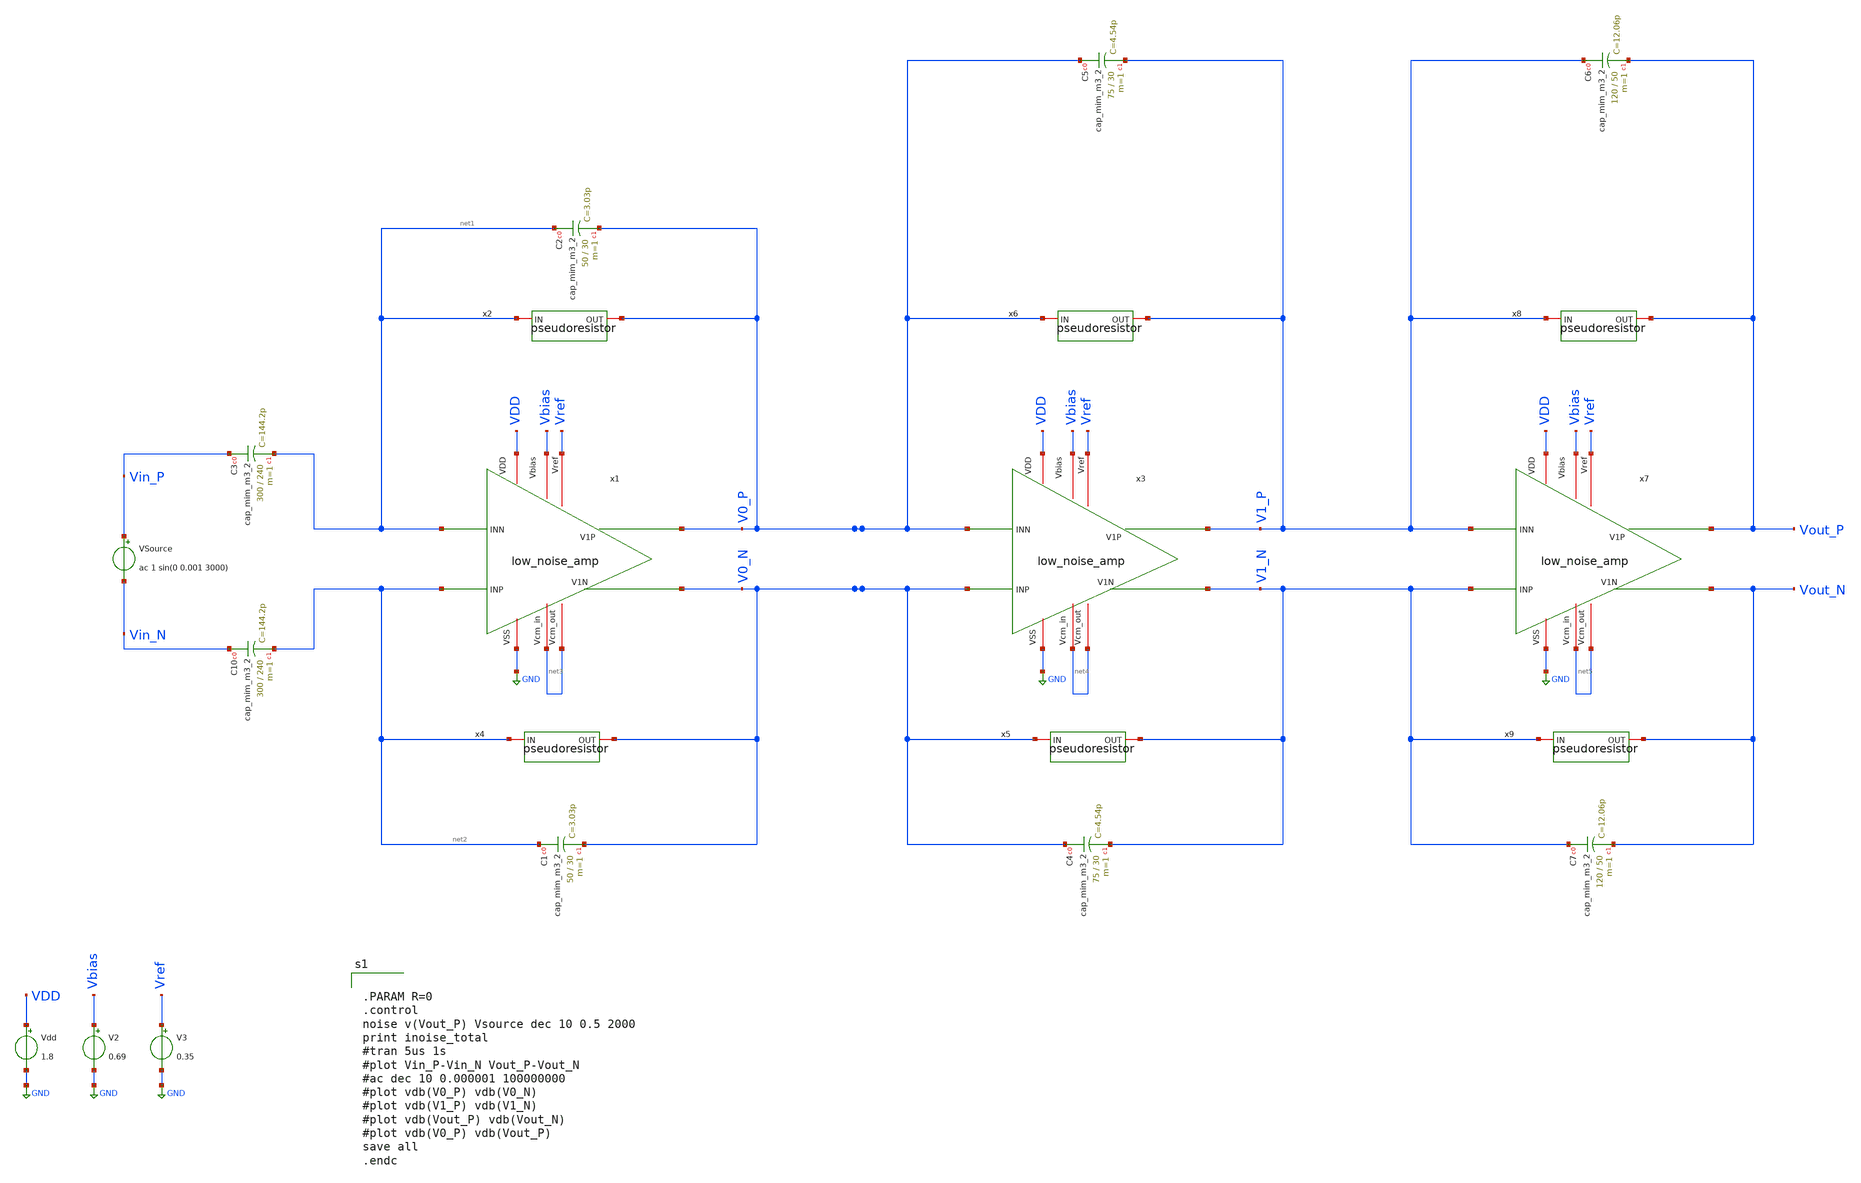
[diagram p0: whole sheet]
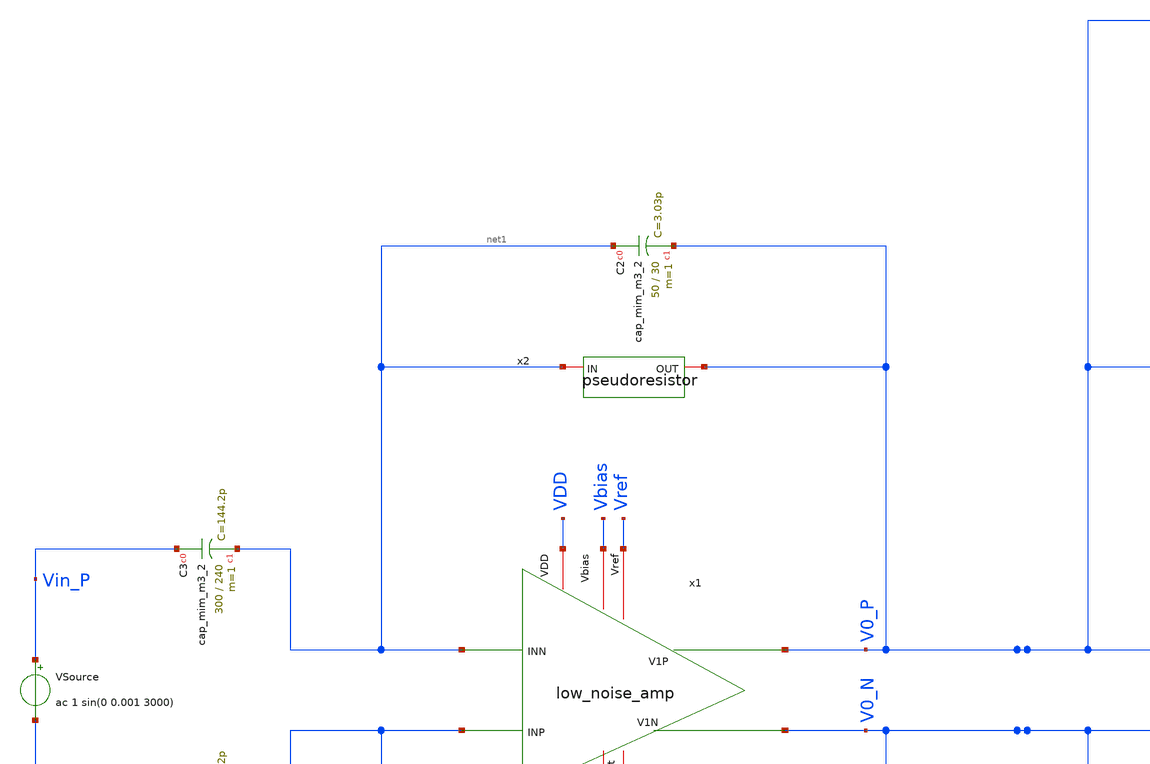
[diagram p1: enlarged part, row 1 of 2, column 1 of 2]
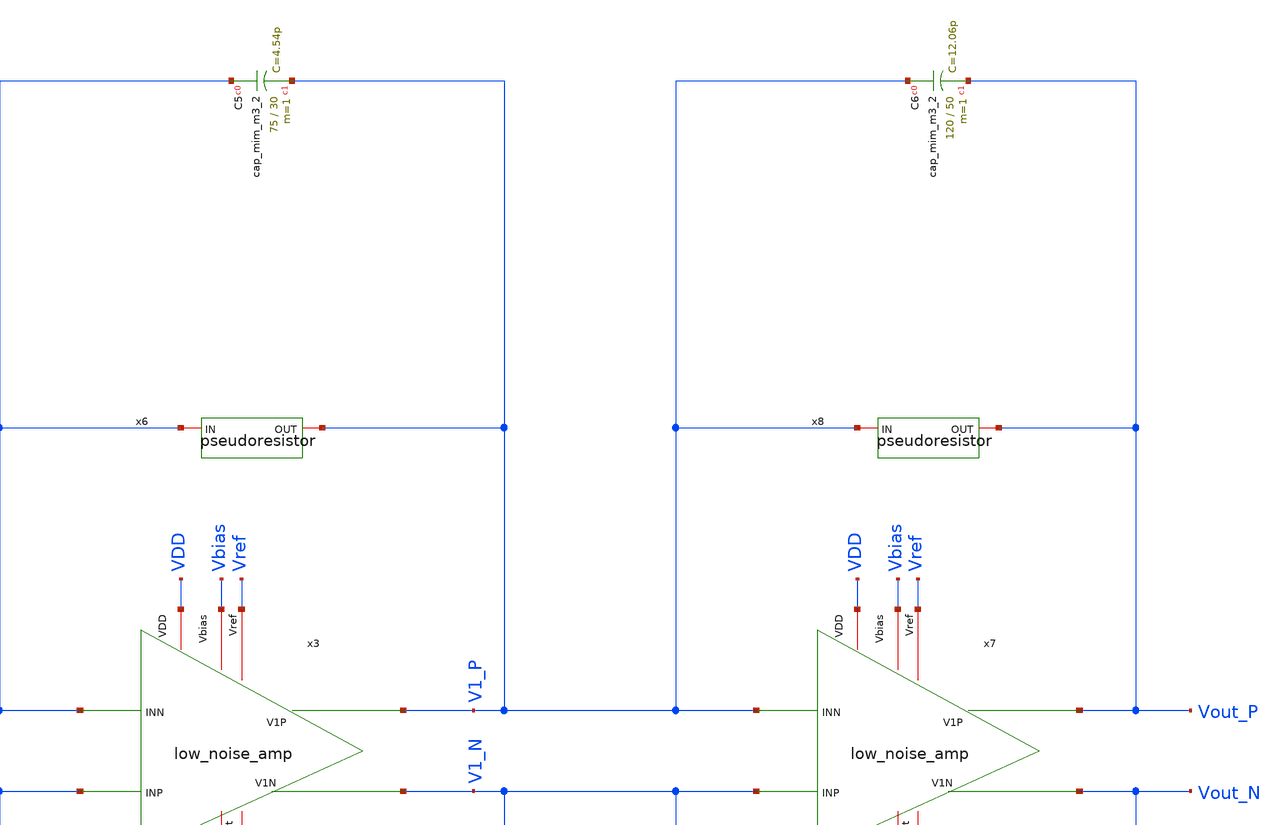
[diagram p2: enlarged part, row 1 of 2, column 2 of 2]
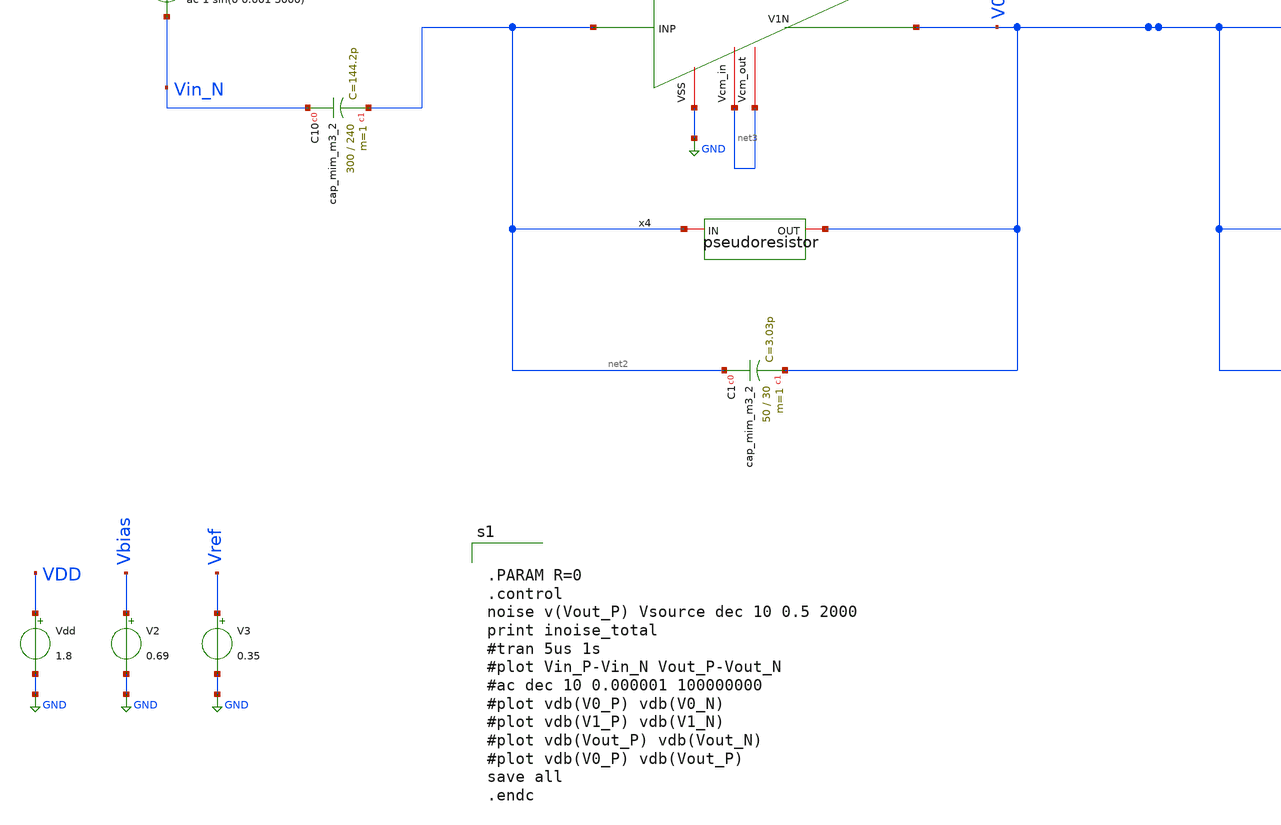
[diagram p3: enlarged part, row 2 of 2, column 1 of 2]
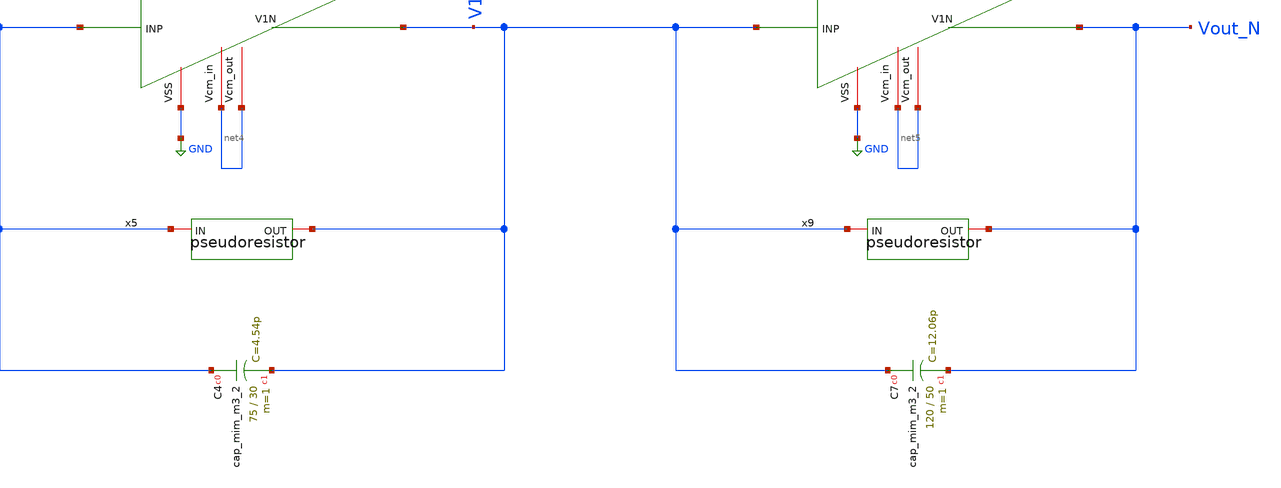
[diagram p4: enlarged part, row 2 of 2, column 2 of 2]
** sch_path: opamp_lna/low_noise_amp_tb_4.sch
**.subckt low_noise_amp_tb_4
x1 VDD net3 net1 net2 V0_P V0_N GND net3 Vbias Vref low_noise_amp
Vdd VDD GND 1.8
V2 Vbias GND 0.69
V3 Vref GND 0.35
VSource Vin_P Vin_N ac 1 sin(0 0.001 3000)
XC1 net2 V0_N sky130_fd_pr__cap_mim_m3_2 W=50 L=30 MF=1 m=1
XC2 net1 V0_P sky130_fd_pr__cap_mim_m3_2 W=50 L=30 MF=1 m=1
x3 VDD net4 V0_P V0_N V1_P V1_N GND net4 Vbias Vref low_noise_amp
x7 VDD net5 V1_P V1_N Vout_P Vout_N GND net5 Vbias Vref low_noise_amp
XC7 V1_N Vout_N sky130_fd_pr__cap_mim_m3_2 W=120 L=50 MF=1 m=1
XC6 V1_P Vout_P sky130_fd_pr__cap_mim_m3_2 W=120 L=50 MF=1 m=1
XC4 V0_N V1_N sky130_fd_pr__cap_mim_m3_2 W=75 L=30 MF=1 m=1
XC5 V0_P V1_P sky130_fd_pr__cap_mim_m3_2 W=75 L=30 MF=1 m=1
x2 net1 V0_P pseudoresistor
x4 net2 V0_N pseudoresistor
x5 V0_N V1_N pseudoresistor
x6 V0_P V1_P pseudoresistor
x8 V1_P Vout_P pseudoresistor
x9 V1_N Vout_N pseudoresistor
XC3 Vin_P net1 sky130_fd_pr__cap_mim_m3_2 W=300 L=240 MF=1 m=1
XC10 Vin_N net2 sky130_fd_pr__cap_mim_m3_2 W=300 L=240 MF=1 m=1
**** begin user architecture code

** opencircuitdesign pdks install
.lib $::SKYWATER_MODELS/sky130.lib.spice tt
.include $::SKYWATER_STDCELLS/sky130_fd_sc_hd.spice



.PARAM R=0
.control
noise v(Vout_P) Vsource dec 10 0.5 2000
print inoise_total
#tran 5us 1s
#plot Vin_P-Vin_N Vout_P-Vout_N
#ac dec 10 0.000001 100000000
#plot vdb(V0_P) vdb(V0_N)
#plot vdb(V1_P) vdb(V1_N)
#plot vdb(Vout_P) vdb(Vout_N)
#plot vdb(V0_P) vdb(Vout_P)
save all
.endc

**** end user architecture code
**.ends

* expanding   symbol:  low_noise_amp.sym # of pins=10
** sym_path: opamp_lna/low_noise_amp.sym
** sch_path: opamp_lna/low_noise_amp.sch
.subckt low_noise_amp VDD Vcm_in INN INP V1P V1N VSS Vcm_out Vbias Vref
*.iopin VDD
*.iopin VSS
*.iopin Vbias
*.ipin INP
*.ipin INN
*.iopin Vref
*.iopin Vcm_in
*.iopin Vcm_out
*.opin V1N
*.opin V1P
XM3 CMFB Vref A0 VDD sky130_fd_pr__pfet_01v8 L=0.8 W=8 nf=1 ad='int((nf+1)/2) * W/nf * 0.29' as='int((nf+2)/2) * W/nf * 0.29'
+ pd='2*int((nf+1)/2) * (W/nf + 0.29)' ps='2*int((nf+2)/2) * (W/nf + 0.29)' nrd='0.29 / W' nrs='0.29 / W'
+ sa=0 sb=0 sd=0 mult=1 m=1
XM11 A0 Vbias VDD VDD sky130_fd_pr__pfet_01v8 L=0.8 W=4 nf=1 ad='int((nf+1)/2) * W/nf * 0.29' as='int((nf+2)/2) * W/nf * 0.29'
+ pd='2*int((nf+1)/2) * (W/nf + 0.29)' ps='2*int((nf+2)/2) * (W/nf + 0.29)' nrd='0.29 / W' nrs='0.29 / W'
+ sa=0 sb=0 sd=0 mult=1 m=1
XM7 V1N INP B0 VDD sky130_fd_pr__pfet_01v8 L=2 W=18 nf=1 ad='int((nf+1)/2) * W/nf * 0.29' as='int((nf+2)/2) * W/nf * 0.29'
+ pd='2*int((nf+1)/2) * (W/nf + 0.29)' ps='2*int((nf+2)/2) * (W/nf + 0.29)' nrd='0.29 / W' nrs='0.29 / W'
+ sa=0 sb=0 sd=0 mult=1 m=1
XM8 V1P INN B0 VDD sky130_fd_pr__pfet_01v8 L=2 W=18 nf=1 ad='int((nf+1)/2) * W/nf * 0.29' as='int((nf+2)/2) * W/nf * 0.29'
+ pd='2*int((nf+1)/2) * (W/nf + 0.29)' ps='2*int((nf+2)/2) * (W/nf + 0.29)' nrd='0.29 / W' nrs='0.29 / W'
+ sa=0 sb=0 sd=0 mult=1 m=1
XM9 V1N INP B1 VSS sky130_fd_pr__nfet_01v8 L=1 W=12 nf=1 ad='int((nf+1)/2) * W/nf * 0.29' as='int((nf+2)/2) * W/nf * 0.29'
+ pd='2*int((nf+1)/2) * (W/nf + 0.29)' ps='2*int((nf+2)/2) * (W/nf + 0.29)' nrd='0.29 / W' nrs='0.29 / W'
+ sa=0 sb=0 sd=0 mult=1 m=1
XM12 B0 Vbias VDD VDD sky130_fd_pr__pfet_01v8 L=0.8 W=4 nf=1 ad='int((nf+1)/2) * W/nf * 0.29' as='int((nf+2)/2) * W/nf * 0.29'
+ pd='2*int((nf+1)/2) * (W/nf + 0.29)' ps='2*int((nf+2)/2) * (W/nf + 0.29)' nrd='0.29 / W' nrs='0.29 / W'
+ sa=0 sb=0 sd=0 mult=1 m=1
XM13 B1 CMFB VSS VSS sky130_fd_pr__nfet_01v8 L=0.8 W=2 nf=1 ad='int((nf+1)/2) * W/nf * 0.29' as='int((nf+2)/2) * W/nf * 0.29'
+ pd='2*int((nf+1)/2) * (W/nf + 0.29)' ps='2*int((nf+2)/2) * (W/nf + 0.29)' nrd='0.29 / W' nrs='0.29 / W'
+ sa=0 sb=0 sd=0 mult=1 m=1
XM15 Vcm_out Vcm_out net1 Vcm_out sky130_fd_pr__pfet_01v8 L=0.6 W=1 nf=1 ad='int((nf+1)/2) * W/nf * 0.29'
+ as='int((nf+2)/2) * W/nf * 0.29' pd='2*int((nf+1)/2) * (W/nf + 0.29)' ps='2*int((nf+2)/2) * (W/nf + 0.29)'
+ nrd='0.29 / W' nrs='0.29 / W' sa=0 sb=0 sd=0 mult=5 m=5
XM16 net1 V1P V1P V1P sky130_fd_pr__pfet_01v8 L=0.6 W=1 nf=1 ad='int((nf+1)/2) * W/nf * 0.29' as='int((nf+2)/2) * W/nf * 0.29'
+ pd='2*int((nf+1)/2) * (W/nf + 0.29)' ps='2*int((nf+2)/2) * (W/nf + 0.29)' nrd='0.29 / W' nrs='0.29 / W'
+ sa=0 sb=0 sd=0 mult=5 m=5
XM17 Vcm_out Vcm_out net2 Vcm_out sky130_fd_pr__pfet_01v8 L=0.6 W=1 nf=1 ad='int((nf+1)/2) * W/nf * 0.29'
+ as='int((nf+2)/2) * W/nf * 0.29' pd='2*int((nf+1)/2) * (W/nf + 0.29)' ps='2*int((nf+2)/2) * (W/nf + 0.29)'
+ nrd='0.29 / W' nrs='0.29 / W' sa=0 sb=0 sd=0 mult=5 m=5
XM18 net2 V1N V1N V1N sky130_fd_pr__pfet_01v8 L=0.6 W=1 nf=1 ad='int((nf+1)/2) * W/nf * 0.29' as='int((nf+2)/2) * W/nf * 0.29'
+ pd='2*int((nf+1)/2) * (W/nf + 0.29)' ps='2*int((nf+2)/2) * (W/nf + 0.29)' nrd='0.29 / W' nrs='0.29 / W'
+ sa=0 sb=0 sd=0 mult=5 m=5
XC1 Vcm_out VSS sky130_fd_pr__cap_mim_m3_1 W=1 L=1 MF=1 m=1
XM1 V1P INN B1 VSS sky130_fd_pr__nfet_01v8 L=1 W=12 nf=1 ad='int((nf+1)/2) * W/nf * 0.29' as='int((nf+2)/2) * W/nf * 0.29'
+ pd='2*int((nf+1)/2) * (W/nf + 0.29)' ps='2*int((nf+2)/2) * (W/nf + 0.29)' nrd='0.29 / W' nrs='0.29 / W'
+ sa=0 sb=0 sd=0 mult=1 m=1
XM2 A1 A1 VSS VSS sky130_fd_pr__nfet_01v8 L=0.8 W=6 nf=1 ad='int((nf+1)/2) * W/nf * 0.29' as='int((nf+2)/2) * W/nf * 0.29'
+ pd='2*int((nf+1)/2) * (W/nf + 0.29)' ps='2*int((nf+2)/2) * (W/nf + 0.29)' nrd='0.29 / W' nrs='0.29 / W'
+ sa=0 sb=0 sd=0 mult=1 m=1
XM5 CMFB A1 VSS VSS sky130_fd_pr__nfet_01v8 L=0.8 W=6 nf=1 ad='int((nf+1)/2) * W/nf * 0.29' as='int((nf+2)/2) * W/nf * 0.29'
+ pd='2*int((nf+1)/2) * (W/nf + 0.29)' ps='2*int((nf+2)/2) * (W/nf + 0.29)' nrd='0.29 / W' nrs='0.29 / W'
+ sa=0 sb=0 sd=0 mult=1 m=1
XM6 A1 Vcm_in A0 VDD sky130_fd_pr__pfet_01v8 L=0.8 W=8 nf=1 ad='int((nf+1)/2) * W/nf * 0.29' as='int((nf+2)/2) * W/nf * 0.29'
+ pd='2*int((nf+1)/2) * (W/nf + 0.29)' ps='2*int((nf+2)/2) * (W/nf + 0.29)' nrd='0.29 / W' nrs='0.29 / W'
+ sa=0 sb=0 sd=0 mult=1 m=1
.ends


* expanding   symbol:  /home/lcg3895/CE393/pseudoresistor.sym # of pins=2
** sym_path: opamp_lna/pseudoresistor.sym
** sch_path: opamp_lna/pseudoresistor.sch
.subckt pseudoresistor IN OUT
*.iopin IN
*.iopin OUT
XM5 net1 IN IN IN sky130_fd_pr__pfet_01v8 L=0.5 W=1 nf=5 ad='int((nf+1)/2) * W/nf * 0.29' as='int((nf+2)/2) * W/nf * 0.29'
+ pd='2*int((nf+1)/2) * (W/nf + 0.29)' ps='2*int((nf+2)/2) * (W/nf + 0.29)' nrd='0.29 / W' nrs='0.29 / W'
+ sa=0 sb=0 sd=0 mult=1 m=1
XM1 net2 net2 net1 net2 sky130_fd_pr__pfet_01v8 L=0.5 W=1 nf=5 ad='int((nf+1)/2) * W/nf * 0.29' as='int((nf+2)/2) * W/nf * 0.29'
+ pd='2*int((nf+1)/2) * (W/nf + 0.29)' ps='2*int((nf+2)/2) * (W/nf + 0.29)' nrd='0.29 / W' nrs='0.29 / W'
+ sa=0 sb=0 sd=0 mult=1 m=1
XM2 net3 net2 net2 net2 sky130_fd_pr__pfet_01v8 L=0.5 W=1 nf=5 ad='int((nf+1)/2) * W/nf * 0.29' as='int((nf+2)/2) * W/nf * 0.29'
+ pd='2*int((nf+1)/2) * (W/nf + 0.29)' ps='2*int((nf+2)/2) * (W/nf + 0.29)' nrd='0.29 / W' nrs='0.29 / W'
+ sa=0 sb=0 sd=0 mult=1 m=1
XM3 OUT OUT net3 OUT sky130_fd_pr__pfet_01v8 L=0.5 W=1 nf=5 ad='int((nf+1)/2) * W/nf * 0.29' as='int((nf+2)/2) * W/nf * 0.29'
+ pd='2*int((nf+1)/2) * (W/nf + 0.29)' ps='2*int((nf+2)/2) * (W/nf + 0.29)' nrd='0.29 / W' nrs='0.29 / W'
+ sa=0 sb=0 sd=0 mult=1 m=1
.ends

.GLOBAL GND
.end
